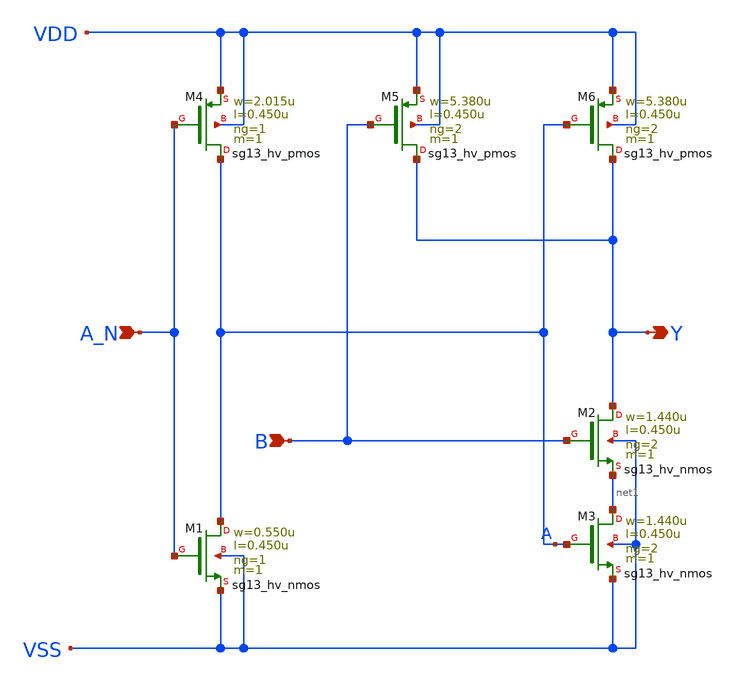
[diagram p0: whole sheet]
** sch_path: ihp-sg13g2/libs.ref/sg13g2_stdcell_hv/sch/xschem/sg13g2_hv_nand2b_2.sch
* Copyright 2023 IHP PDK Authors
* Licensed under the Apache License, Version 2.0 (the "License");
* you may not use this file except in compliance with the License.
* You may obtain a copy of the License at
* https://www.apache.org/licenses/LICENSE-2.0
* Unless required by applicable law or agreed to in writing, software
* distributed under the License is distributed on an "AS IS" BASIS,
* WITHOUT WARRANTIES OR CONDITIONS OF ANY KIND, either express or implied.
* See the License for the specific language governing permissions and
* limitations under the License.
**.subckt sg13g2_hv_nand2b_2 Y B A_N
*.opin Y
*.ipin B
*.ipin A_N
XM1 A A_N VSS VSS sg13_hv_nmos w=0.550u l=0.450u ng=1 m=1 mm_ok=1
XM2 Y B net1 VSS sg13_hv_nmos w=1.440u l=0.450u ng=2 m=1 mm_ok=1
XM3 net1 A VSS VSS sg13_hv_nmos w=1.440u l=0.450u ng=2 m=1 mm_ok=1
XM4 A A_N VDD VDD sg13_hv_pmos w=2.015u l=0.450u ng=1 m=1 mm_ok=1
XM5 Y B VDD VDD sg13_hv_pmos w=5.380u l=0.450u ng=2 m=1 mm_ok=1
XM6 Y A VDD VDD sg13_hv_pmos w=5.380u l=0.450u ng=2 m=1 mm_ok=1
**.ends
.end
